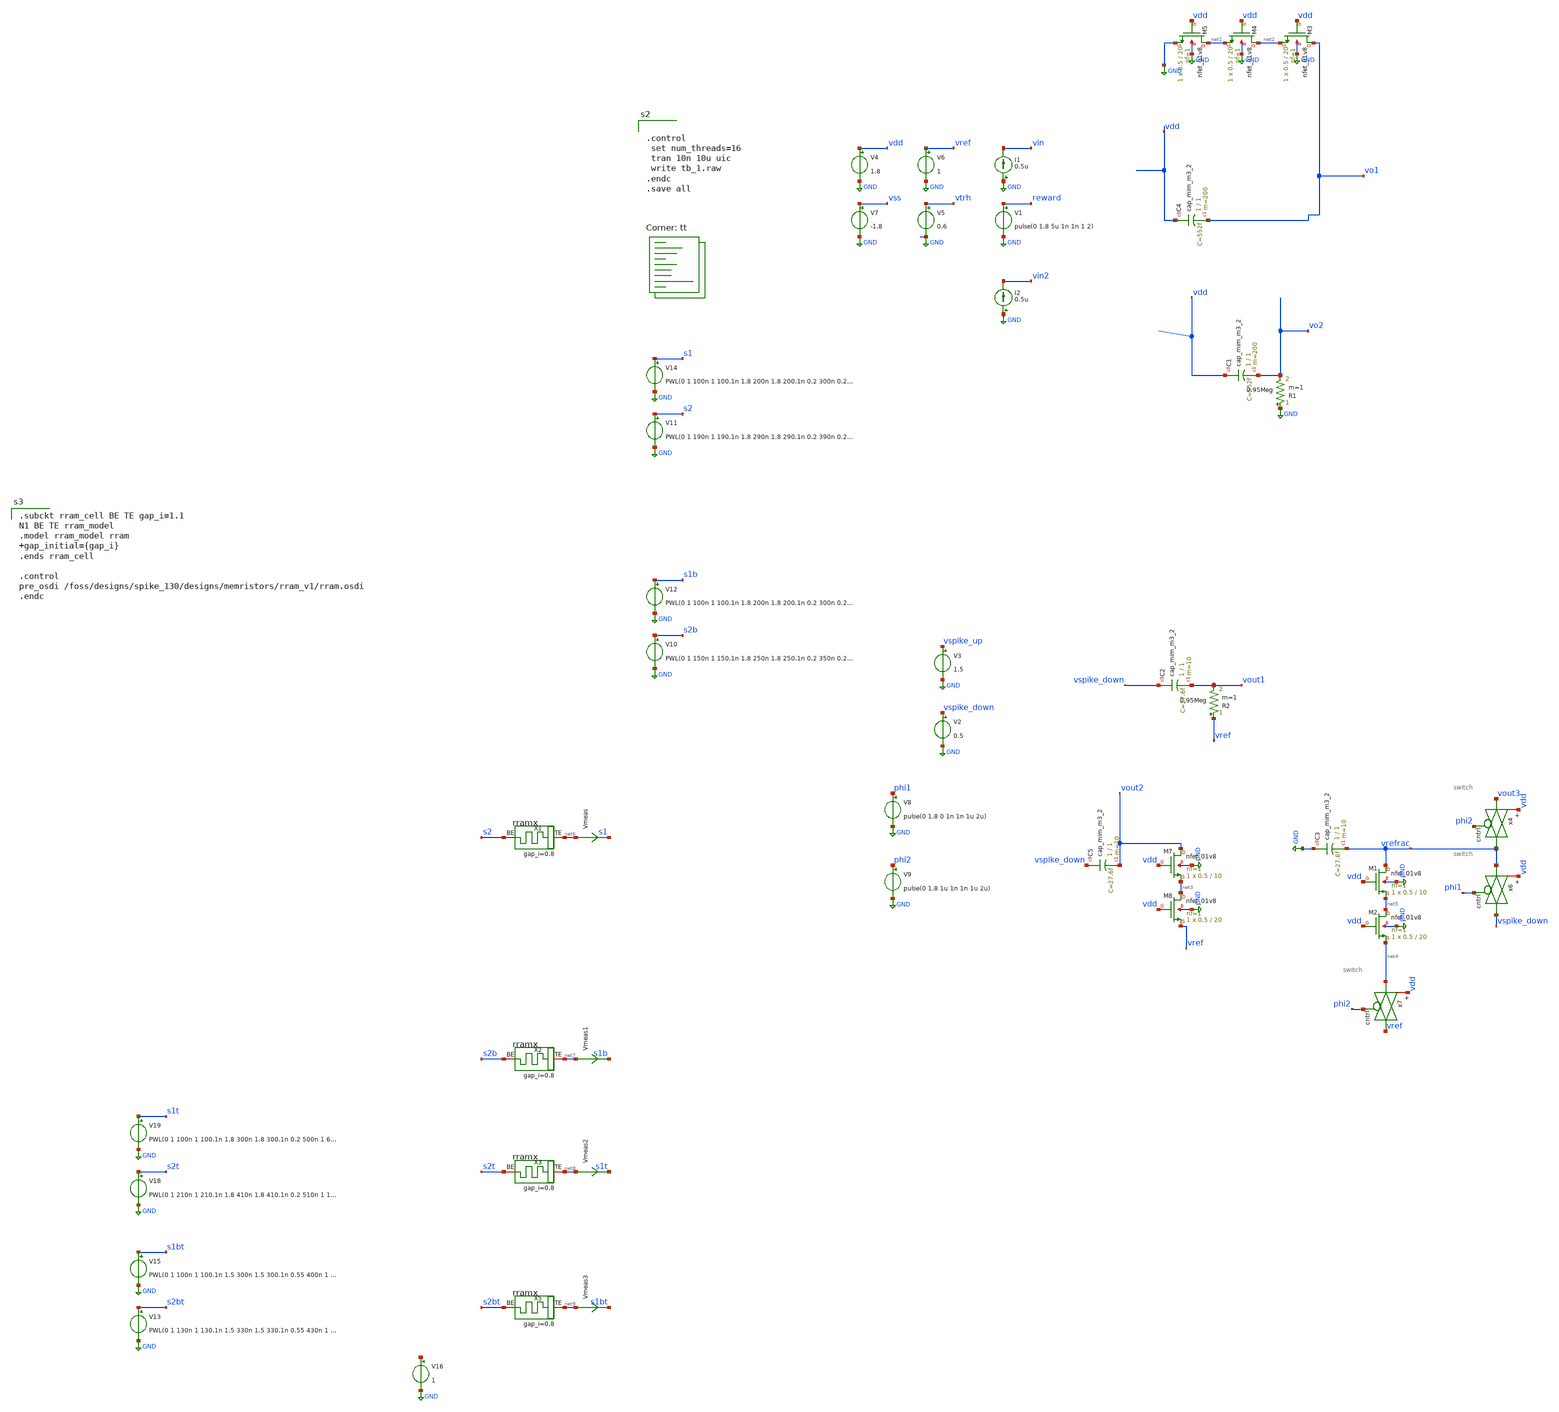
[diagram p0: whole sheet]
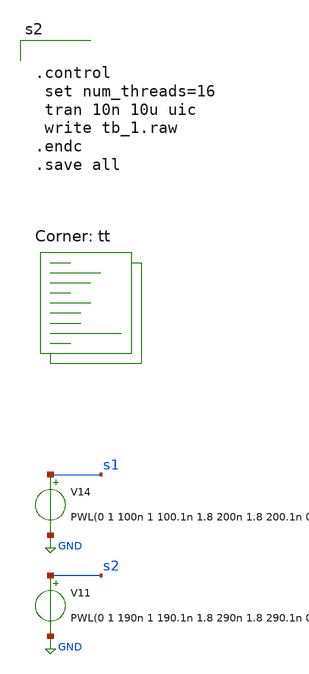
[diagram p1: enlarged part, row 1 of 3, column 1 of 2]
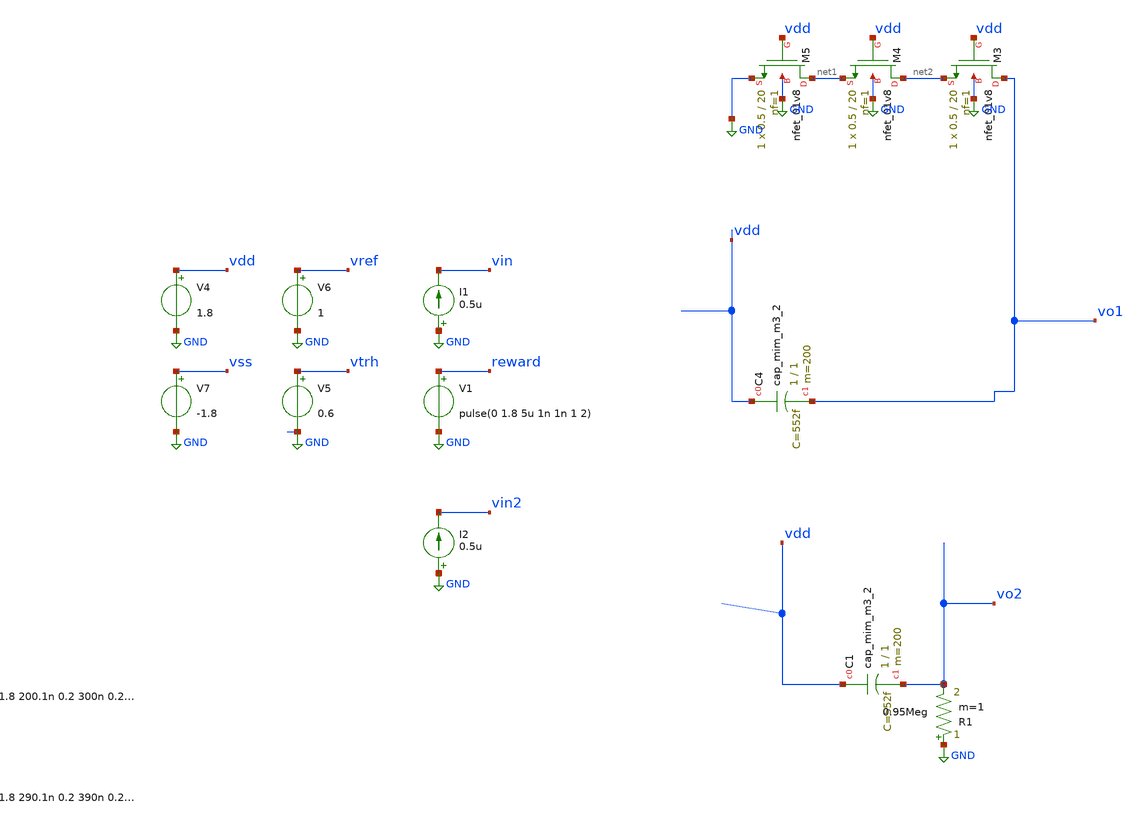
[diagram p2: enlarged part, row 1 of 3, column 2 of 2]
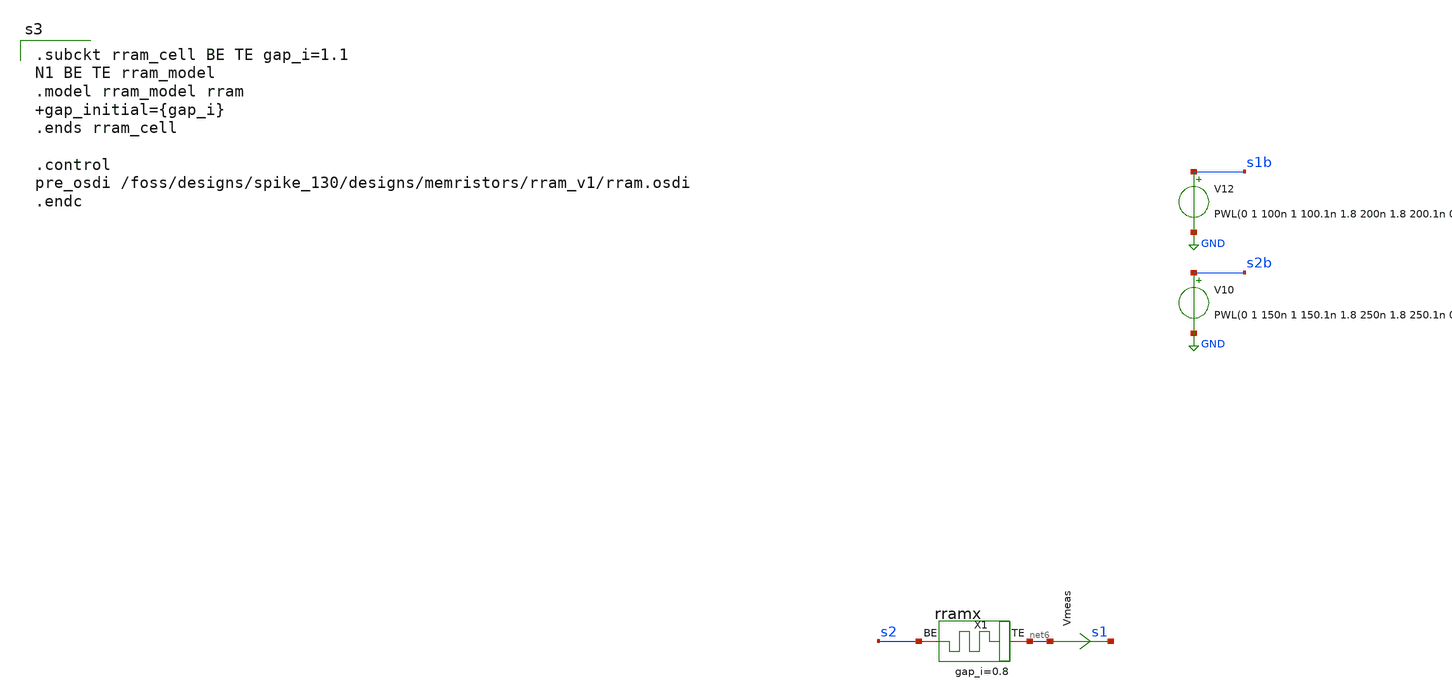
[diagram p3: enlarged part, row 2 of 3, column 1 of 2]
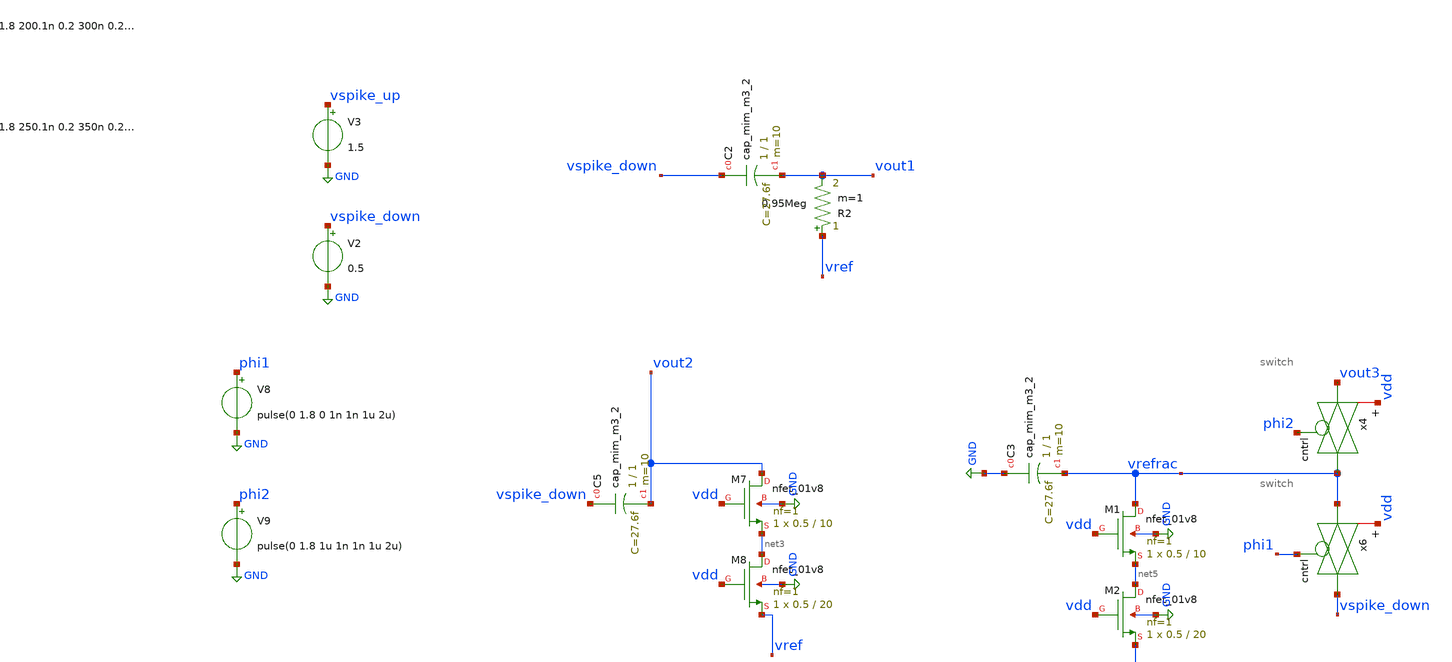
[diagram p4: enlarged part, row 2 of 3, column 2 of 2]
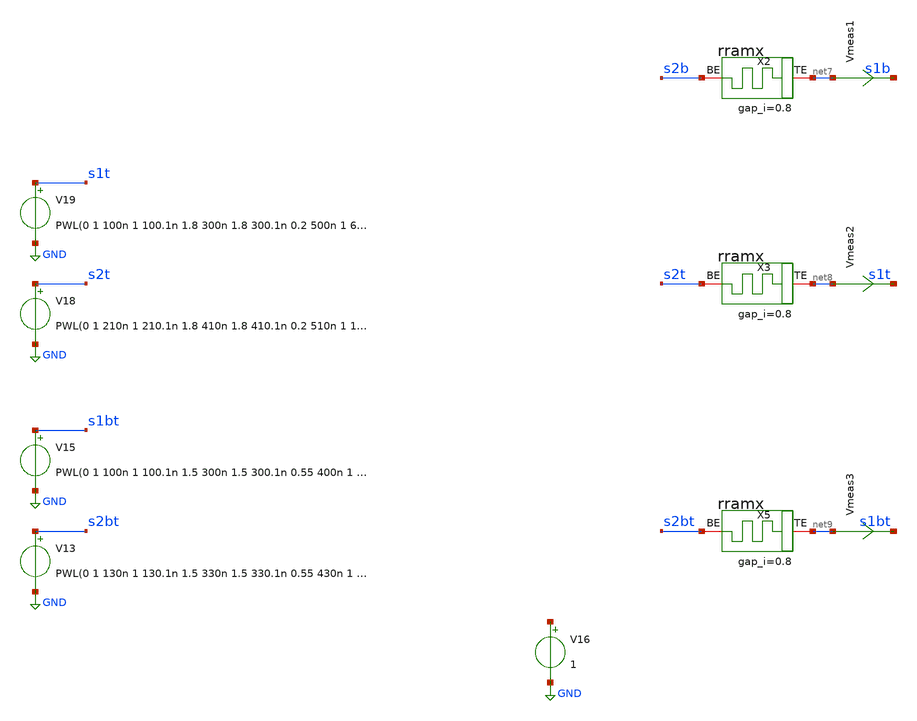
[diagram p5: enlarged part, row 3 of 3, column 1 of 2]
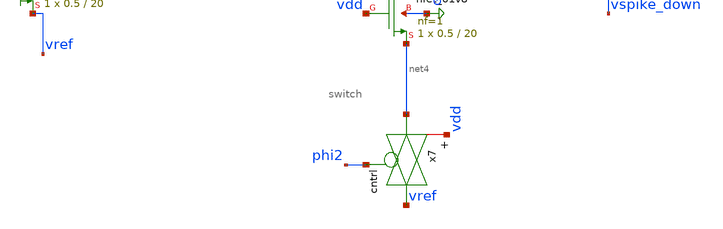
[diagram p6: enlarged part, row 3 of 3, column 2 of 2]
** sch_path: designs/tb_1.sch
**.subckt tb_1
V4 vdd GND 1.8
V5 vtrh GND 0.6
V6 vref GND 1
I1 GND vin 0.5u
V7 vss GND -1.8
V1 reward GND pulse(0 1.8 5u 1n 1n 1 2)
XC4 vdd vo1 sky130_fd_pr__cap_mim_m3_2 W=1 L=1 MF=200 m=200
XM3 vo1 vdd net2 GND sky130_fd_pr__nfet_01v8 L=20 W=0.5 nf=1 ad='int((1 + 1)/2) * 0.5 / 1 * 0.29' as='int((1 + 2)/2) * 0.5 / 1 * 0.29'
+ pd='2*int((1 + 1)/2) * (0.5 / 1 + 0.29)' ps='2*int((1 + 2)/2) * (0.5 / 1 + 0.29)' nrd='0.29 / 0.5 ' nrs='0.29 / 0.5 '
+ sa=0 sb=0 sd=0 mult=1 m=1
XM4 net2 vdd net1 GND sky130_fd_pr__nfet_01v8 L=20 W=0.5 nf=1 ad='int((1 + 1)/2) * 0.5 / 1 * 0.29' as='int((1 + 2)/2) * 0.5 / 1 * 0.29'
+ pd='2*int((1 + 1)/2) * (0.5 / 1 + 0.29)' ps='2*int((1 + 2)/2) * (0.5 / 1 + 0.29)' nrd='0.29 / 0.5 ' nrs='0.29 / 0.5 '
+ sa=0 sb=0 sd=0 mult=1 m=1
XM5 net1 vdd GND GND sky130_fd_pr__nfet_01v8 L=20 W=0.5 nf=1 ad='int((1 + 1)/2) * 0.5 / 1 * 0.29' as='int((1 + 2)/2) * 0.5 / 1 * 0.29'
+ pd='2*int((1 + 1)/2) * (0.5 / 1 + 0.29)' ps='2*int((1 + 2)/2) * (0.5 / 1 + 0.29)' nrd='0.29 / 0.5 ' nrs='0.29 / 0.5 '
+ sa=0 sb=0 sd=0 mult=1 m=1
XC1 vdd vo2 sky130_fd_pr__cap_mim_m3_2 W=1 L=1 MF=200 m=200
R1 GND vo2 0.95Meg m=1
I2 GND vin2 0.5u
V2 vspike_down GND 0.5
V3 vspike_up GND 1.5
R2 vref vout1 0.95Meg m=1
XM7 vout2 vdd net3 GND sky130_fd_pr__nfet_01v8 L=10 W=0.5 nf=1 ad='int((1 + 1)/2) * 0.5 / 1 * 0.29' as='int((1 + 2)/2) * 0.5 / 1 * 0.29'
+ pd='2*int((1 + 1)/2) * (0.5 / 1 + 0.29)' ps='2*int((1 + 2)/2) * (0.5 / 1 + 0.29)' nrd='0.29 / 0.5 ' nrs='0.29 / 0.5 '
+ sa=0 sb=0 sd=0 mult=1 m=1
XM8 net3 vdd vref GND sky130_fd_pr__nfet_01v8 L=20 W=0.5 nf=1 ad='int((1 + 1)/2) * 0.5 / 1 * 0.29' as='int((1 + 2)/2) * 0.5 / 1 * 0.29'
+ pd='2*int((1 + 1)/2) * (0.5 / 1 + 0.29)' ps='2*int((1 + 2)/2) * (0.5 / 1 + 0.29)' nrd='0.29 / 0.5 ' nrs='0.29 / 0.5 '
+ sa=0 sb=0 sd=0 mult=1 m=1
XC5 vspike_down vout2 sky130_fd_pr__cap_mim_m3_2 W=1 L=1 MF=10 m=10
XC2 vspike_down vout1 sky130_fd_pr__cap_mim_m3_2 W=1 L=1 MF=10 m=10
XC3 GND vrefrac sky130_fd_pr__cap_mim_m3_2 W=1 L=1 MF=10 m=10
XM1 vrefrac vdd net5 GND sky130_fd_pr__nfet_01v8 L=10 W=0.5 nf=1 ad='int((1 + 1)/2) * 0.5 / 1 * 0.29'
+ as='int((1 + 2)/2) * 0.5 / 1 * 0.29' pd='2*int((1 + 1)/2) * (0.5 / 1 + 0.29)' ps='2*int((1 + 2)/2) * (0.5 / 1 + 0.29)'
+ nrd='0.29 / 0.5 ' nrs='0.29 / 0.5 ' sa=0 sb=0 sd=0 mult=1 m=1
x4 phi2 vout3 vrefrac vdd switch
x6 phi1 vrefrac vspike_down vdd switch
x7 phi2 net4 vref vdd switch
XM2 net5 vdd net4 GND sky130_fd_pr__nfet_01v8 L=20 W=0.5 nf=1 ad='int((1 + 1)/2) * 0.5 / 1 * 0.29' as='int((1 + 2)/2) * 0.5 / 1 * 0.29'
+ pd='2*int((1 + 1)/2) * (0.5 / 1 + 0.29)' ps='2*int((1 + 2)/2) * (0.5 / 1 + 0.29)' nrd='0.29 / 0.5 ' nrs='0.29 / 0.5 '
+ sa=0 sb=0 sd=0 mult=1 m=1
V8 phi1 GND pulse(0 1.8 0 1n 1n 1u 2u)
V9 phi2 GND pulse(0 1.8 1u 1n 1n 1u 2u)
V11 s2 GND PWL(0 1 190n 1 190.1n 1.8 290n 1.8 290.1n 0.2 390n 0.2 390.1n 1 1000n 1 r=0)
V14 s1 GND PWL(0 1 100n 1 100.1n 1.8 200n 1.8 200.1n 0.2 300n 0.2 300.1n 1 500n 1 r=0)
Vmeas net6 s1 0
.save i(vmeas)
X1 net6 s2 rram_cell gap_i=0.8
Vmeas1 net7 s1b 0
.save i(vmeas1)
X2 net7 s2b rram_cell gap_i=0.8
V10 s2b GND PWL(0 1 150n 1 150.1n 1.8 250n 1.8 250.1n 0.2 350n 0.2 350.1n 1 1000n 1 r=0)
V12 s1b GND PWL(0 1 100n 1 100.1n 1.8 200n 1.8 200.1n 0.2 300n 0.2 300.1n 1 500n 1 r=0)
Vmeas2 net8 s1t 0
.save i(vmeas2)
X3 net8 s2t rram_cell gap_i=0.8
Vmeas3 net9 s1bt 0
.save i(vmeas3)
X5 net9 s2bt rram_cell gap_i=0.8
V18 s2t GND PWL(0 1 210n 1 210.1n 1.8 410n 1.8 410.1n 0.2 510n 1 1200n 1 r=0)
V19 s1t GND PWL(0 1 100n 1 100.1n 1.8 300n 1.8 300.1n 0.2 500n 1 600n 1 r=0)
V13 s2bt GND PWL(0 1 130n 1 130.1n 1.5 330n 1.5 330.1n 0.55 430n 1 1000n 1 r=0)
V15 s1bt GND PWL(0 1 100n 1 100.1n 1.5 300n 1.5 300.1n 0.55 400n 1 500n 1 r=0)
V16 net10 GND 1
**** begin user architecture code


.control
 set num_threads=16
 tran 10n 10u uic
 write tb_1.raw
.endc
.save all

.lib $::SKYWATER_MODELS/sky130.lib.spice tt

.subckt rram_cell BE TE gap_i=1.1
N1 BE TE rram_model
.model rram_model rram gap_initial={gap_i}
.ends rram_cell

.control
pre_osdi /foss/designs/spike_130/designs/memristors/rram_v1/rram.osdi
.endc

**** end user architecture code
**.ends

* expanding   symbol:  /foss/designs/spike_130/designs/subcells/core_switch/switch.sym # of pins=4
** sym_path: designs/subcells/core_switch/switch.sym
** sch_path: designs/subcells/core_switch/switch.sch
.subckt switch cntrl in out vdd
*.ipin cntrl
*.ipin in
*.iopin vdd
*.opin out
XM3 out cntrl in GND sky130_fd_pr__nfet_01v8 L=0.15 W=1 nf=1 ad='int((1 + 1)/2) * 1 / 1 * 0.29' as='int((1 + 2)/2) * 1 / 1 * 0.29'
+ pd='2*int((1 + 1)/2) * (1 / 1 + 0.29)' ps='2*int((1 + 2)/2) * (1 / 1 + 0.29)' nrd='0.29 / 1 ' nrs='0.29 / 1 '
+ sa=0 sb=0 sd=0 mult=1 m=1
XM4 out net1 in vdd sky130_fd_pr__pfet_01v8 L=0.15 W=1 nf=1 ad='int((nf+1)/2) * W/nf * 0.29' as='int((nf+2)/2) * W/nf * 0.29'
+ pd='2*int((nf+1)/2) * (W/nf + 0.29)' ps='2*int((nf+2)/2) * (W/nf + 0.29)' nrd='0.29 / W' nrs='0.29 / W'
+ sa=0 sb=0 sd=0 mult=1 m=1
x1 vdd cntrl net1 not
.ends


* expanding   symbol:  /foss/designs/spike_130/designs/subcells/core_not/not.sym # of pins=3
** sym_path: designs/subcells/core_not/not.sym
** sch_path: designs/subcells/core_not/not.sch
.subckt not vdd in out
*.ipin in
*.opin out
*.iopin vdd
XM10 out in vdd vdd sky130_fd_pr__pfet_01v8_lvt L=0.35 W=1 nf=1 ad='int((1 + 1)/2) * 1 / 1 * 0.29' as='int((1 + 2)/2) * 1 / 1 * 0.29'
+ pd='2*int((1 + 1)/2) * (1 / 1 + 0.29)' ps='2*int((1 + 2)/2) * (1 / 1 + 0.29)' nrd='0.29 / 1 ' nrs='0.29 / 1 '
+ sa=0 sb=0 sd=0 mult=1 m=1
XM1 out in GND GND sky130_fd_pr__nfet_01v8_lvt L=0.15 W=1 nf=1 ad='int((1 + 1)/2) * 1 / 1 * 0.29' as='int((1 + 2)/2) * 1 / 1 * 0.29'
+ pd='2*int((1 + 1)/2) * (1 / 1 + 0.29)' ps='2*int((1 + 2)/2) * (1 / 1 + 0.29)' nrd='0.29 / 1 ' nrs='0.29 / 1 '
+ sa=0 sb=0 sd=0 mult=1 m=1
.ends

.GLOBAL GND
.end
